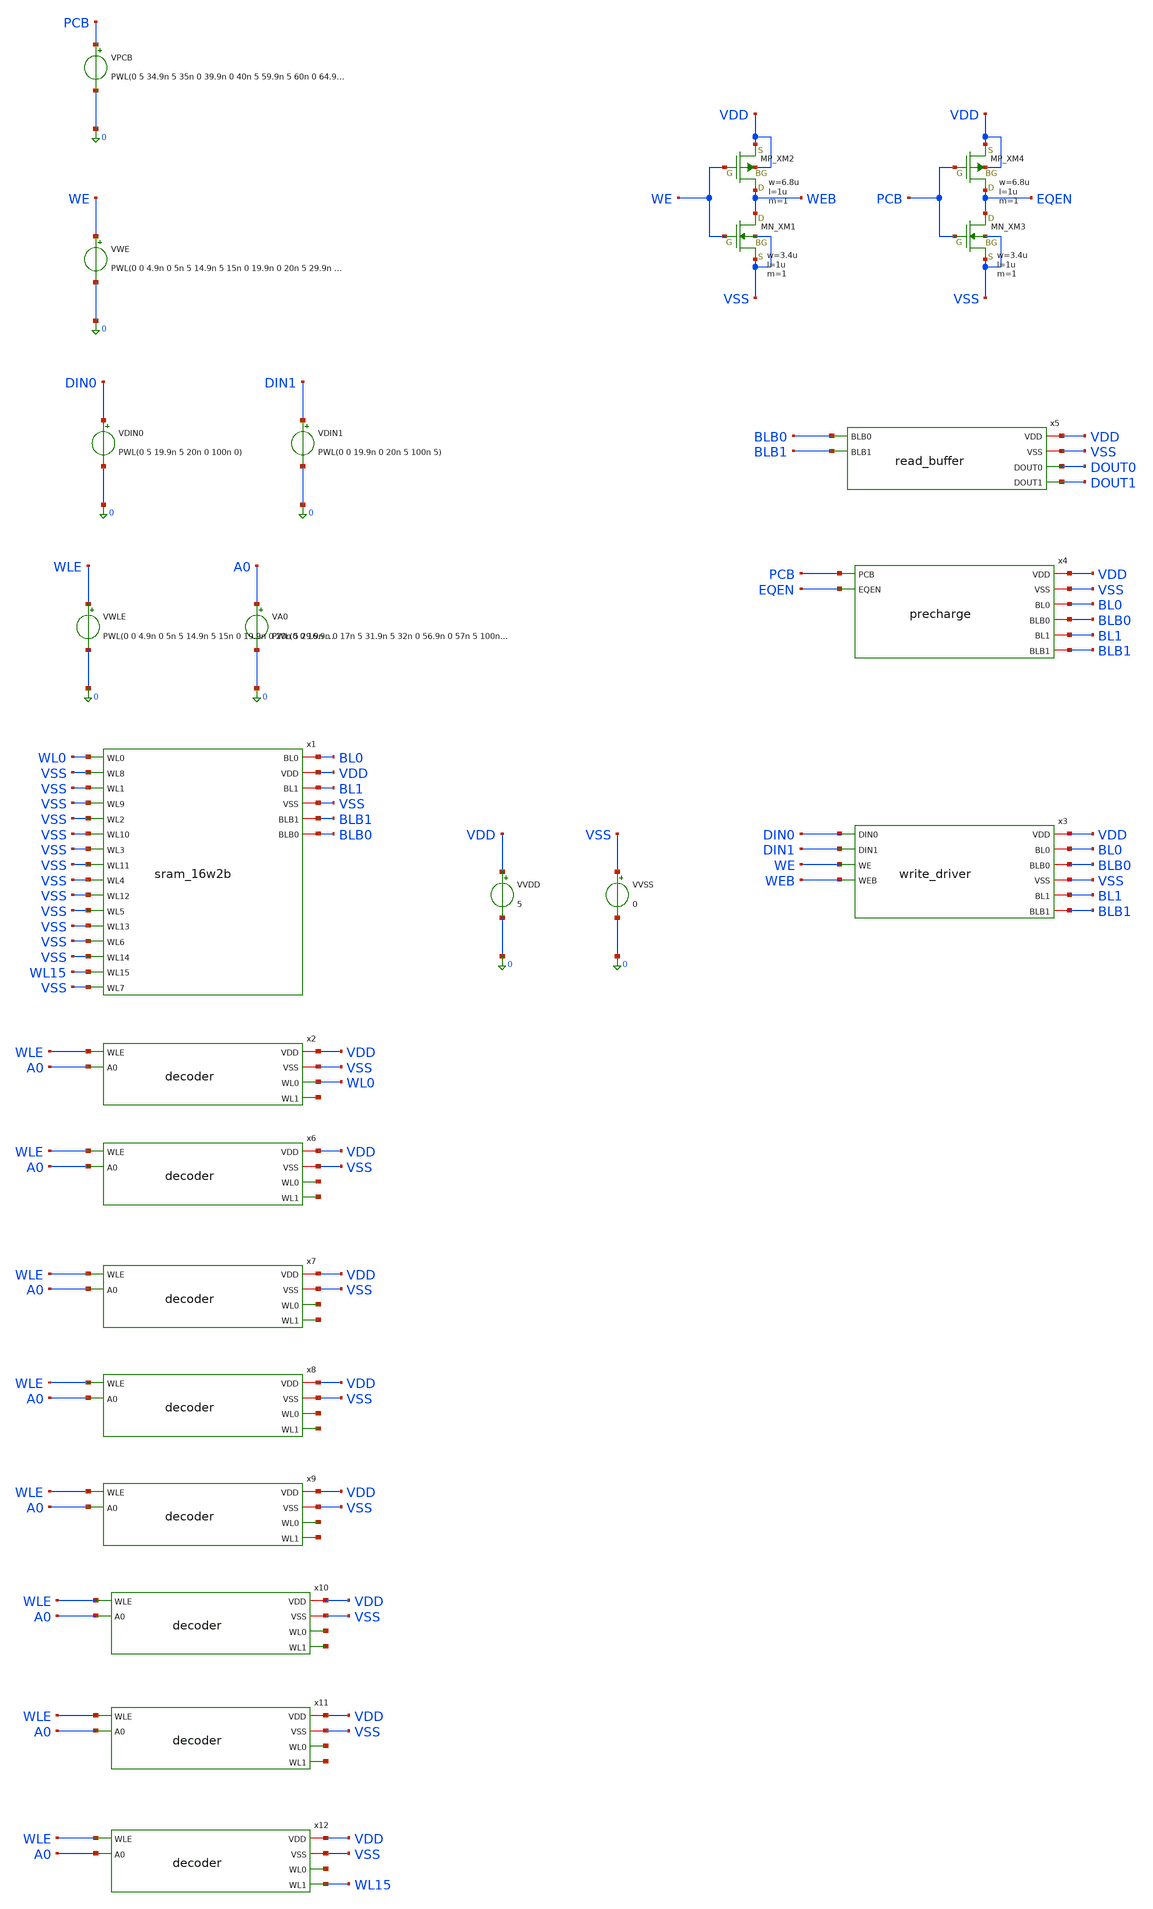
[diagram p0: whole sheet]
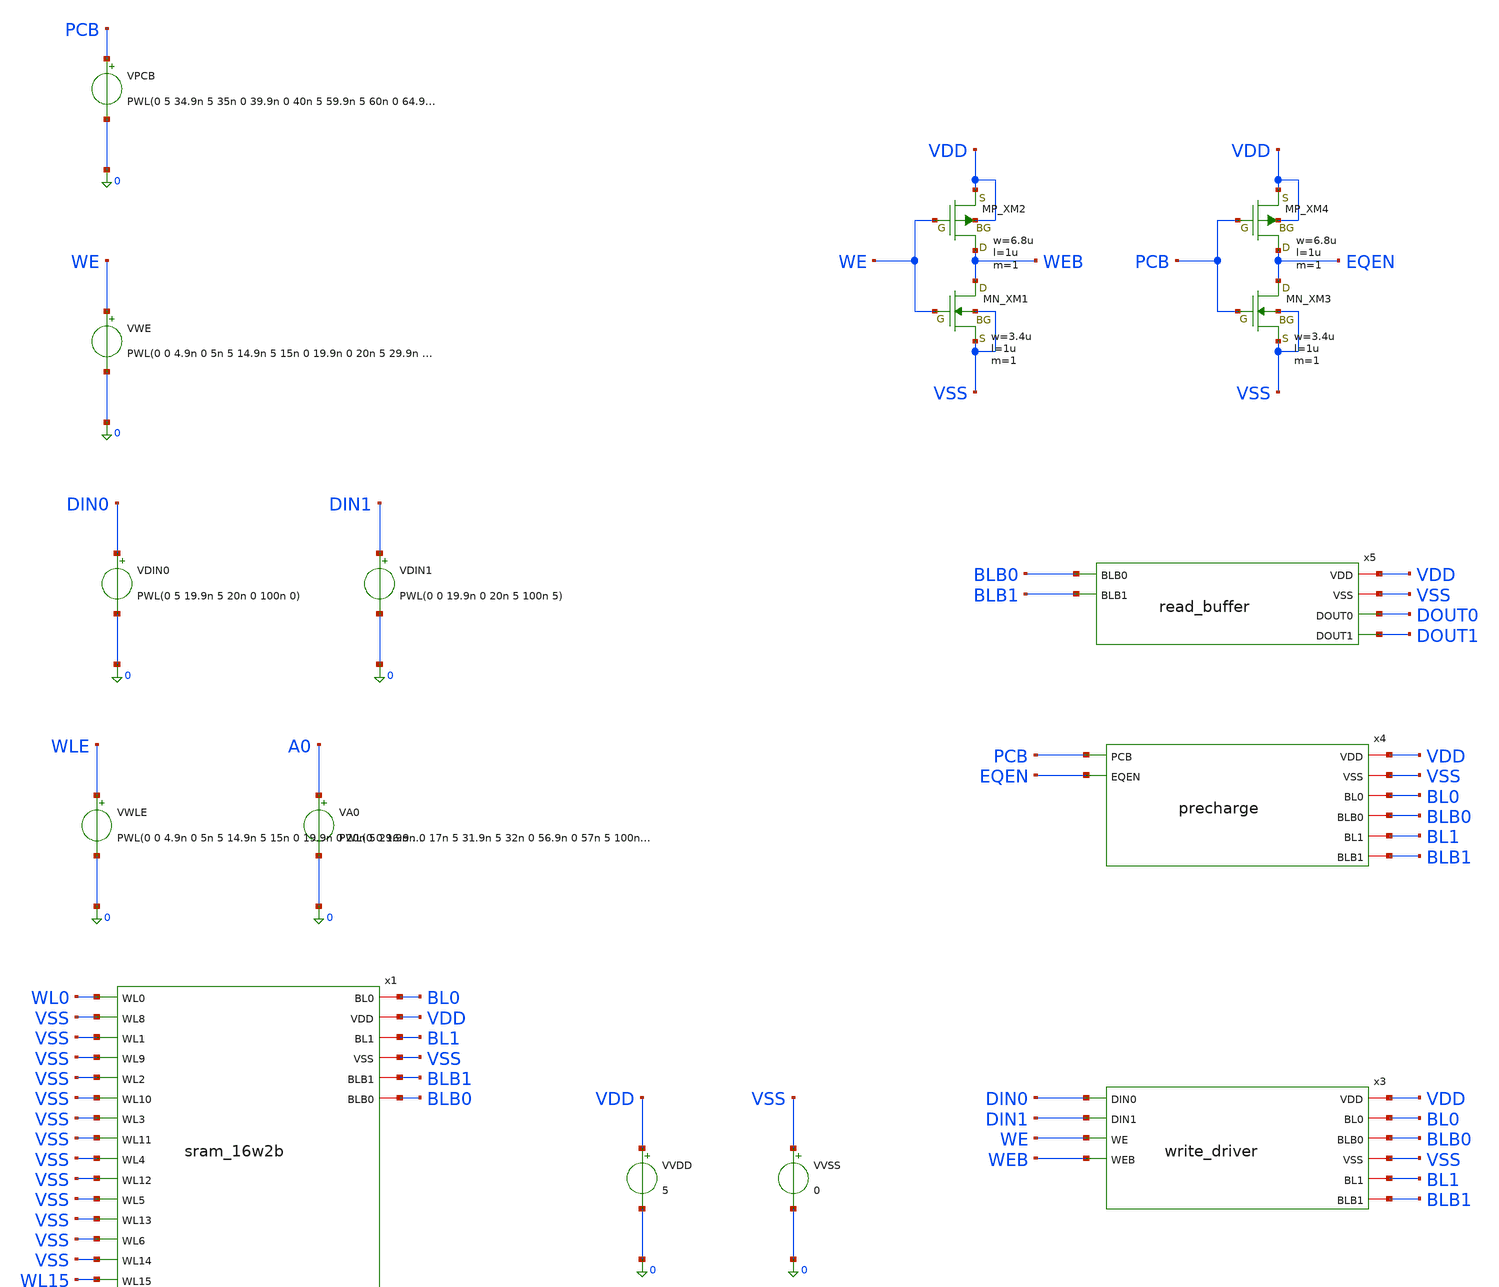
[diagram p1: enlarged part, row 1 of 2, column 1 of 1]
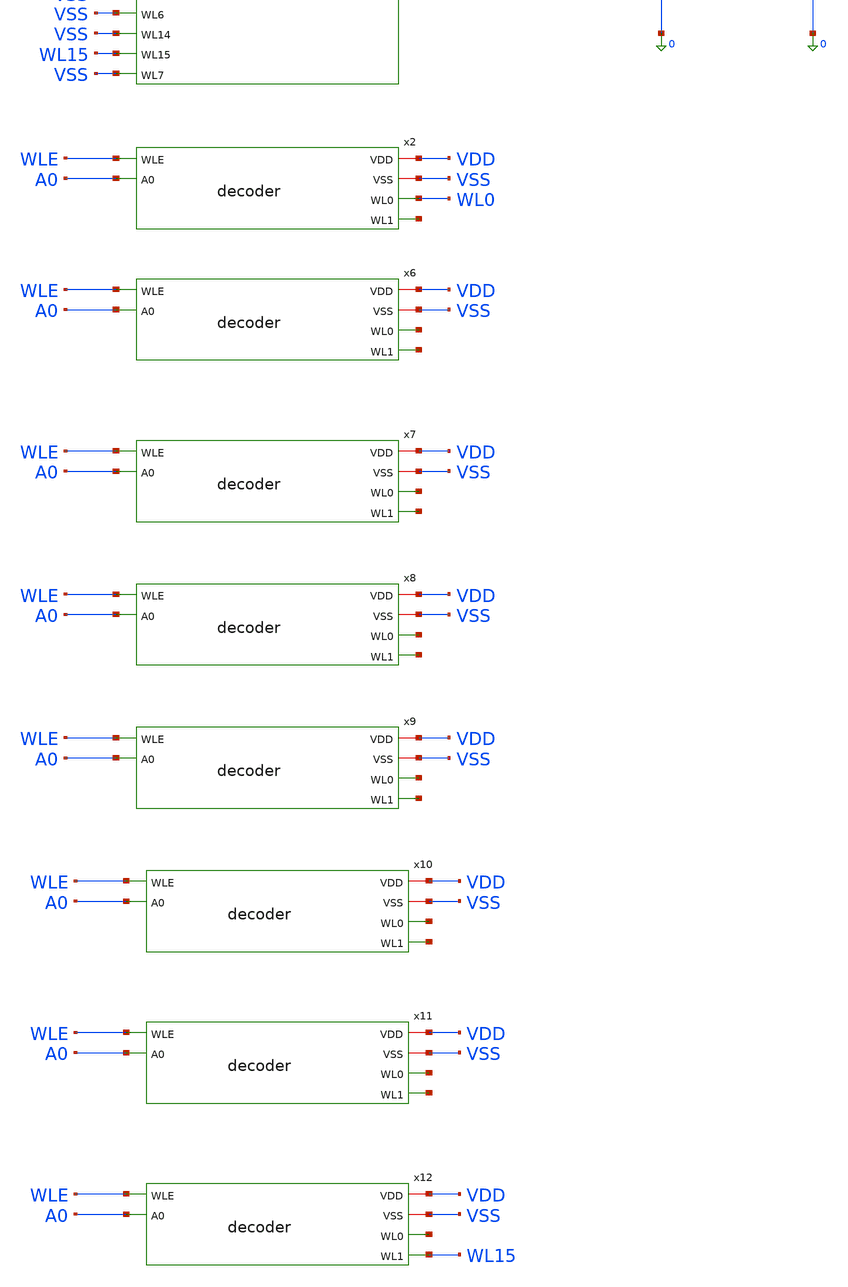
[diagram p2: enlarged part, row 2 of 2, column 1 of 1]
** sch_path: sram/tb_sram_16w2b_test.sch
**.subckt tb_sram_16w2b_test
VVDD VDD 0 5
VDIN0 DIN0 0 PWL(0 5 19.9n 5 20n 0 100n 0)
VVSS VSS 0 0
VWE WE 0 PWL(0 0 4.9n 0 5n 5 14.9n 5 15n 0 19.9n 0 20n 5 29.9n 5 30n 0 100n 0)
VPCB PCB 0 PWL(0 5 34.9n 5 35n 0 39.9n 0 40n 5 59.9n 5 60n 0 64.9n 0 65n 5 100n 5)
x2 VDD VSS WL0 WLE A0 net1 decoder
VWLE WLE 0 PWL(0 0 4.9n 0 5n 5 14.9n 5 15n 0 19.9n 0 20n 5 29.9n 5 30n 0 44.9n 0 45n 5 54.9n 5 55n 0
+ 69.9n 0 70n 5 79.9n 5 80n 0 100n 0)
VA0 A0 0 PWL(0 0 16.9n 0 17n 5 31.9n 5 32n 0 56.9n 0 57n 5 100n 5)
x3 DIN0 VDD BL0 BLB0 VSS DIN1 BL1 WE BLB1 WEB write_driver
VDIN1 DIN1 0 PWL(0 0 19.9n 0 20n 5 100n 5)
x4 VDD VSS PCB EQEN BL0 BLB0 BL1 BLB1 precharge
x5 VDD VSS BLB0 BLB1 DOUT0 DOUT1 read_buffer
XXM1 WEB WE VSS VSS NMOS w=3.4u l=1u nrd=0 nrs=0 m=1
XXM2 WEB WE VDD VDD PMOS w=6.8u l=1u nrd=0 nrs=0 m=1
XXM3 EQEN PCB VSS VSS NMOS w=3.4u l=1u nrd=0 nrs=0 m=1
XXM4 EQEN PCB VDD VDD PMOS w=6.8u l=1u nrd=0 nrs=0 m=1
x1 BL0 VDD WL0 VSS BL1 VSS VSS BLB1 VSS BLB0 VSS VSS VSS VSS VSS VSS VSS VSS VSS VSS WL15 VSS
+ sram_16w2b
x6 VDD VSS net2 WLE A0 net3 decoder
x7 VDD VSS net4 WLE A0 net5 decoder
x8 VDD VSS net6 WLE A0 net7 decoder
x9 VDD VSS net8 WLE A0 net9 decoder
x10 VDD VSS net10 WLE A0 net11 decoder
x11 VDD VSS net12 WLE A0 net13 decoder
x12 VDD VSS net14 WLE A0 WL15 decoder
**** begin user architecture code
 .include $::LIB/ip62_models



.tran 10p 100n

* ============================================================
* RowMax 16w2b SRAM Read Measurement
* Active rows: WL0 and WL15
* Observe: bit0 and bit1
* ============================================================

* ---- WL0 read ----
.meas tran t_wl0_rise WHEN v(WL0)=2.5 RISE=2
.meas tran t_dout0_rise WHEN v(DOUT0)=2.5 RISE=1 TD=40n
.meas tran td_read0 PARAM='t_dout0_rise-t_wl0_rise'

* ---- WL15 read ----
.meas tran t_wl15_rise WHEN v(WL15)=2.5 RISE=2
.meas tran t_dout1_rise WHEN v(DOUT1)=2.5 RISE=1 TD=65n
.meas tran td_read15 PARAM='t_dout1_rise-t_wl15_rise'

* ---- BL differential (temporary fixed-time measurement) ----
.meas tran dvbl0_05 FIND par('abs(v(BL0)-v(BLB0))') AT=46.88n
.meas tran dvbl0_10 FIND par('abs(v(BL0)-v(BLB0))') AT=47.38n

.meas tran dvbl1_05 FIND par('abs(v(BL1)-v(BLB1))') AT=46.88n
.meas tran dvbl1_10 FIND par('abs(v(BL1)-v(BLB1))') AT=47.38n

.control
run

plot v(pcb) v(eqen)+6
plot v(wl0) v(wl15)+6
plot v(dout0)+12 v(dout1)+18
plot v(bl0) v(blb0)
plot v(bl1) v(blb1)

.endc


**** end user architecture code
**.ends
.end
